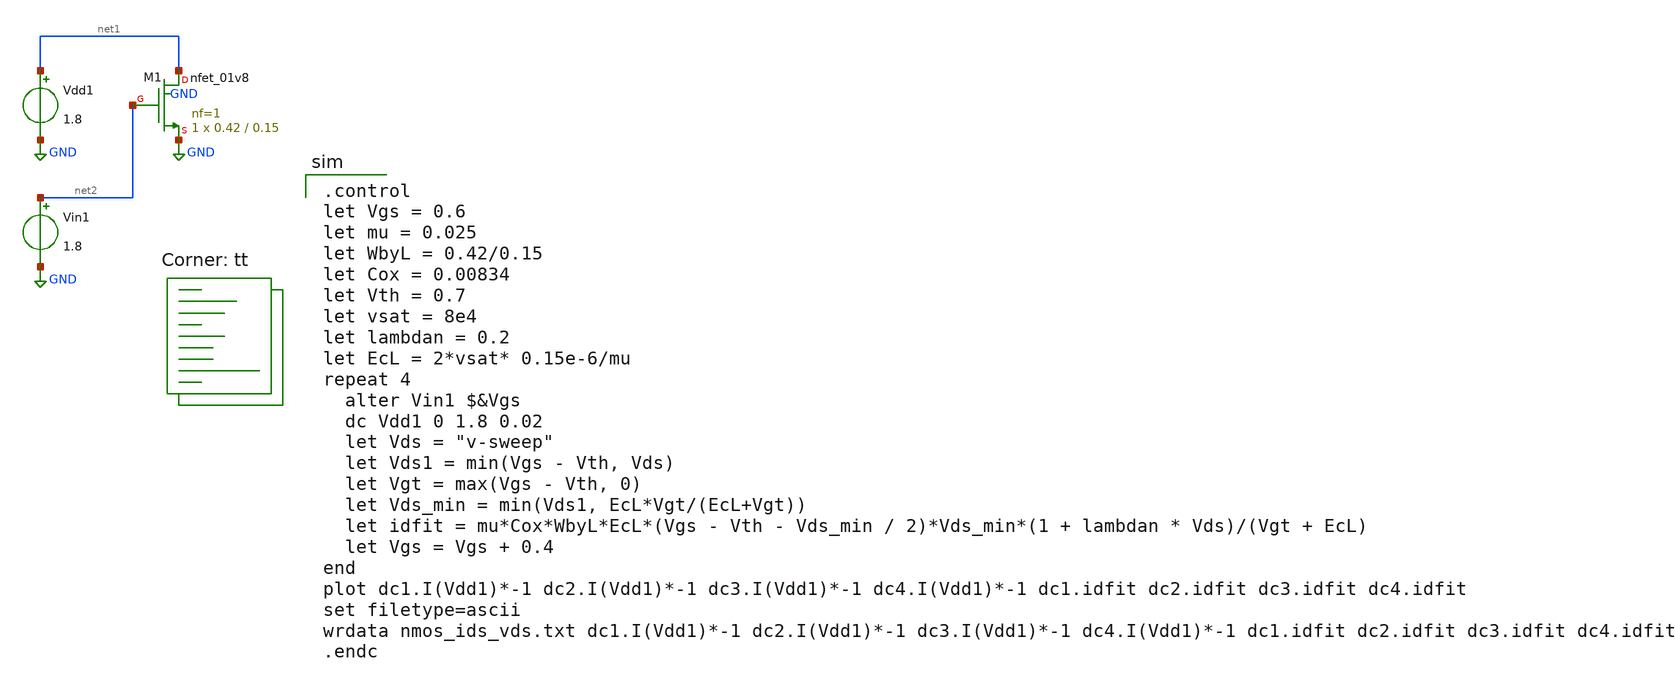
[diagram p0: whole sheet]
** sch_path: tutorial_2/tutorial_2_1b.sch
**.subckt tutorial_2_1b
XM1 net1 net2 GND GND sky130_fd_pr__nfet_01v8 L=0.15 W=0.42 nf=1 ad='int((nf+1)/2) * W/nf * 0.29' as='int((nf+2)/2) * W/nf * 0.29'
+ pd='2*int((nf+1)/2) * (W/nf + 0.29)' ps='2*int((nf+2)/2) * (W/nf + 0.29)' nrd='0.29 / W' nrs='0.29 / W'
+ sa=0 sb=0 sd=0 mult=1 m=1
Vdd1 net1 GND 1.8
Vin1 net2 GND 1.8
**** begin user architecture code

.control
let Vgs = 0.6
let mu = 0.025
let WbyL = 0.42/0.15
let Cox = 0.00834
let Vth = 0.7
let vsat = 8e4
let lambdan = 0.2
let EcL = 2*vsat* 0.15e-6/mu
repeat 4
  alter Vin1 $&Vgs
  dc Vdd1 0 1.8 0.02
  let Vds = "v-sweep"
  let Vds1 = min(Vgs - Vth, Vds)
  let Vgt = max(Vgs - Vth, 0)
  let Vds_min = min(Vds1, EcL*Vgt/(EcL+Vgt))
  let idfit = mu*Cox*WbyL*EcL*(Vgs - Vth - Vds_min / 2)*Vds_min*(1 + lambdan * Vds)/(Vgt + EcL)
  let Vgs = Vgs + 0.4
end
plot dc1.I(Vdd1)*-1 dc2.I(Vdd1)*-1 dc3.I(Vdd1)*-1 dc4.I(Vdd1)*-1 dc1.idfit dc2.idfit dc3.idfit
+ dc4.idfit
set filetype=ascii
wrdata nmos_ids_vds.txt dc1.I(Vdd1)*-1 dc2.I(Vdd1)*-1 dc3.I(Vdd1)*-1 dc4.I(Vdd1)*-1 dc1.idfit
+ dc2.idfit dc3.idfit dc4.idfit
.endc

.lib $::SKYWATER_MODELS/sky130.lib.spice tt
**** end user architecture code
**.ends
.GLOBAL GND
.end
